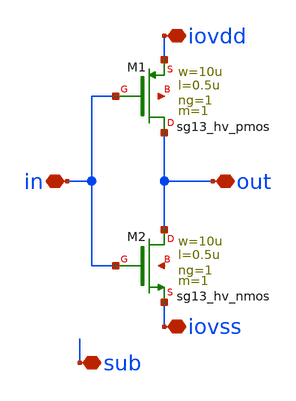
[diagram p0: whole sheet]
** sch_path: libs.tech/xschem/hm_stdcells/sg13g2_io_inv_hv_noptap.sch
**.subckt sg13g2_io_inv_hv_noptap out iovdd iovss sub in
*.iopin out
*.iopin iovdd
*.iopin iovss
*.iopin sub
*.iopin in
XM1 out in iovdd net1 sg13_hv_pmos w=10u l=0.5u ng=1 m=1 mm_ok=1
XM2 out in iovss net2 sg13_hv_nmos w=10u l=0.5u ng=1 m=1 mm_ok=1
**.ends
.end
